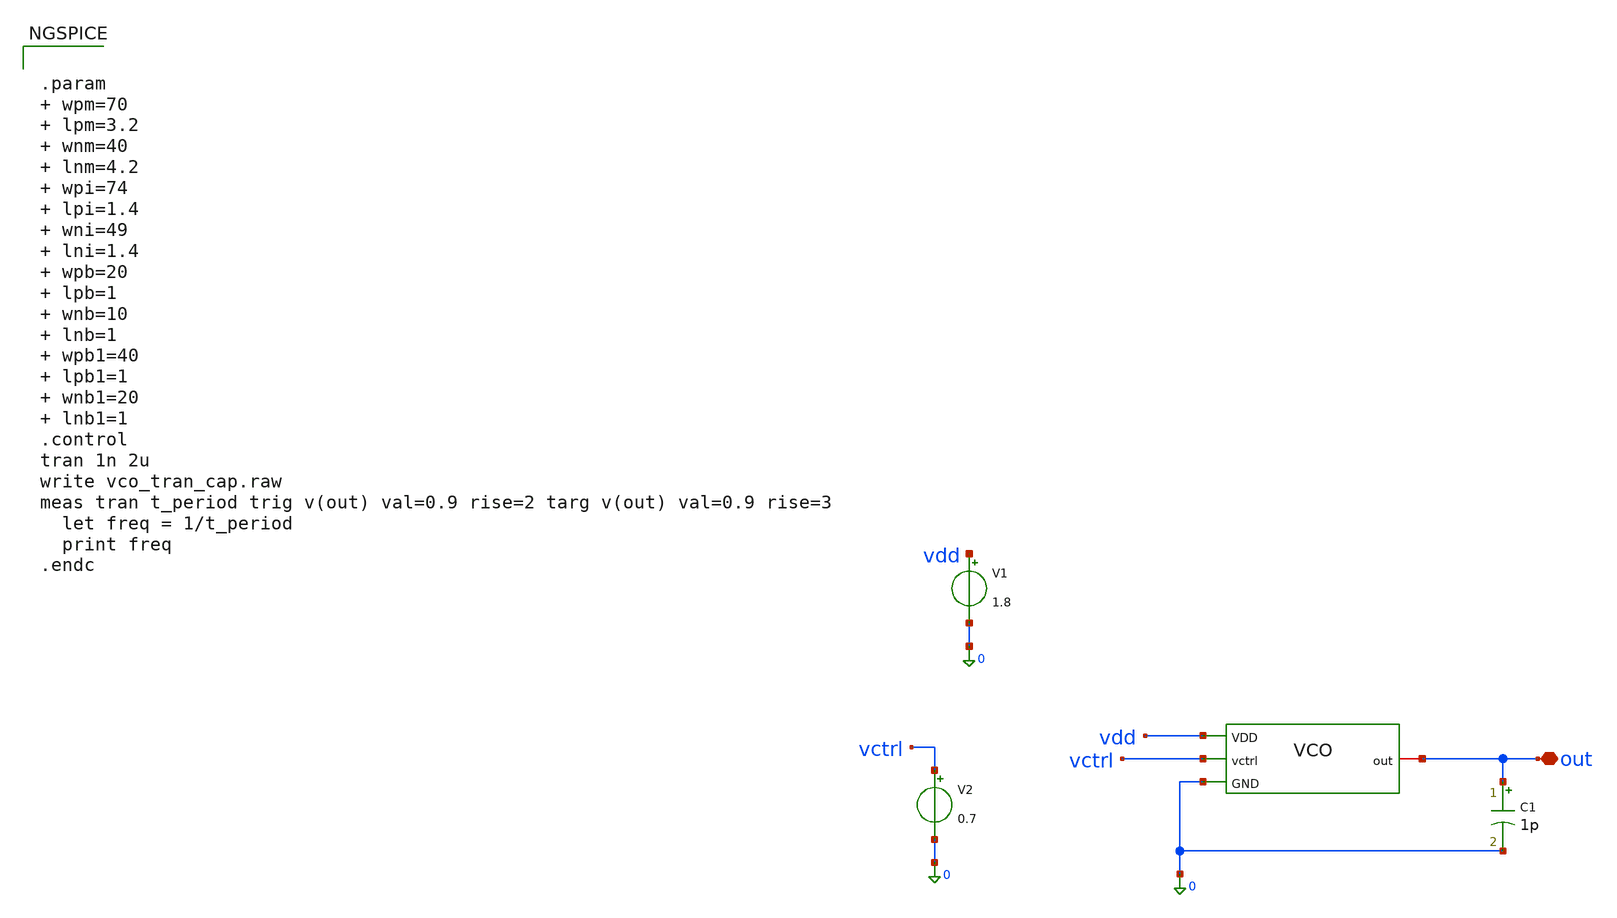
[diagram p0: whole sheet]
** sch_path: design_data/xschem/VCO/vco_tran_cap.sch
**.subckt vco_tran_cap out
*.iopin out
V1 vdd 0 1.8
V2 vctrl 0 0.7
C1 out 0 1p m=1
x1 vdd out vctrl 0 vco
**** begin user architecture code


.param  wpm=70  lpm=3.2  wnm=40  lnm=4.2  wpi=74  lpi=1.4  wni=49  lni=1.4  wpb=20  lpb=1  wnb=10
+  lnb=1  wpb1=40  lpb1=1  wnb1=20  lnb1=1
.control
tran 1n 2u
write vco_tran_cap.raw
meas tran t_period trig v(out) val=0.9 rise=2 targ v(out) val=0.9 rise=3
  let freq = 1/t_period
  print freq
.endc



** opencircuitdesign pdks install
.lib $::SKYWATER_MODELS/sky130.lib.spice ss

**** end user architecture code
**.ends

* expanding   symbol:  xschem/VCO/vco.sym # of pins=4
** sym_path: design_data/xschem/VCO/vco.sym
** sch_path: design_data/xschem/VCO/vco.sch
.subckt vco VDD out vctrl GND
*.ipin vctrl
*.iopin out
*.ipin GND
*.ipin VDD
XM7 net4 net4 VDD VDD sky130_fd_pr__pfet_01v8 L=3.2 W=70 nf=1 ad='int((1 + 1)/2) * 70 / 1 * 0.29' as='int((1 + 2)/2) * 70 / 1 * 0.29'
+ pd='2*int((1 + 1)/2) * (70 / 1 + 0.29)' ps='2*int((1 + 2)/2) * (70 / 1 + 0.29)' nrd='0.29 / 70 ' nrs='0.29 / 70 '
+ sa=0 sb=0 sd=0 mult=1 m=1
XM8 net4 vctrl GND GND sky130_fd_pr__nfet_01v8 L=4.2 W=40 nf=1 ad='int((1 + 1)/2) * 40 / 1 * 0.29' as='int((1 + 2)/2) * 40 / 1 * 0.29'
+ pd='2*int((1 + 1)/2) * (40 / 1 + 0.29)' ps='2*int((1 + 2)/2) * (40 / 1 + 0.29)' nrd='0.29 / 40 ' nrs='0.29 / 40 '
+ sa=0 sb=0 sd=0 mult=1 m=1
XM5 net11 vctrl GND GND sky130_fd_pr__nfet_01v8 L=4.2 W=40 nf=1 ad='int((1 + 1)/2) * 40 / 1 * 0.29' as='int((1 + 2)/2) * 40 / 1 * 0.29'
+ pd='2*int((1 + 1)/2) * (40 / 1 + 0.29)' ps='2*int((1 + 2)/2) * (40 / 1 + 0.29)' nrd='0.29 / 40 ' nrs='0.29 / 40 '
+ sa=0 sb=0 sd=0 mult=1 m=1
XM6 net1 net3 net11 GND sky130_fd_pr__nfet_01v8 L=1.4 W=49 nf=1 ad='int((1 + 1)/2) * 49 / 1 * 0.29' as='int((1 + 2)/2) * 49 / 1 * 0.29'
+ pd='2*int((1 + 1)/2) * (49 / 1 + 0.29)' ps='2*int((1 + 2)/2) * (49 / 1 + 0.29)' nrd='0.29 / 49 ' nrs='0.29 / 49 '
+ sa=0 sb=0 sd=0 mult=1 m=1
XM1 net2 net4 VDD VDD sky130_fd_pr__pfet_01v8 L=3.2 W=70 nf=1 ad='int((1 + 1)/2) * 70 / 1 * 0.29' as='int((1 + 2)/2) * 70 / 1 * 0.29'
+ pd='2*int((1 + 1)/2) * (70 / 1 + 0.29)' ps='2*int((1 + 2)/2) * (70 / 1 + 0.29)' nrd='0.29 / 70 ' nrs='0.29 / 70 '
+ sa=0 sb=0 sd=0 mult=1 m=1
XM2 net1 net3 net2 net2 sky130_fd_pr__pfet_01v8 L=1.4 W=74 nf=1 ad='int((1 + 1)/2) * 74 / 1 * 0.29' as='int((1 + 2)/2) * 74 / 1 * 0.29'
+ pd='2*int((1 + 1)/2) * (74 / 1 + 0.29)' ps='2*int((1 + 2)/2) * (74 / 1 + 0.29)' nrd='0.29 / 74 ' nrs='0.29 / 74 '
+ sa=0 sb=0 sd=0 mult=1 m=1
XM3 net10 vctrl GND GND sky130_fd_pr__nfet_01v8 L=4.2 W=40 nf=1 ad='int((1 + 1)/2) * 40 / 1 * 0.29' as='int((1 + 2)/2) * 40 / 1 * 0.29'
+ pd='2*int((1 + 1)/2) * (40 / 1 + 0.29)' ps='2*int((1 + 2)/2) * (40 / 1 + 0.29)' nrd='0.29 / 40 ' nrs='0.29 / 40 '
+ sa=0 sb=0 sd=0 mult=1 m=1
XM9 net5 net4 VDD VDD sky130_fd_pr__pfet_01v8 L=3.2 W=70 nf=1 ad='int((1 + 1)/2) * 70 / 1 * 0.29' as='int((1 + 2)/2) * 70 / 1 * 0.29'
+ pd='2*int((1 + 1)/2) * (70 / 1 + 0.29)' ps='2*int((1 + 2)/2) * (70 / 1 + 0.29)' nrd='0.29 / 70 ' nrs='0.29 / 70 '
+ sa=0 sb=0 sd=0 mult=1 m=1
XM11 net9 vctrl GND GND sky130_fd_pr__nfet_01v8 L=4.2 W=40 nf=1 ad='int((1 + 1)/2) * 40 / 1 * 0.29' as='int((1 + 2)/2) * 40 / 1 * 0.29'
+ pd='2*int((1 + 1)/2) * (40 / 1 + 0.29)' ps='2*int((1 + 2)/2) * (40 / 1 + 0.29)' nrd='0.29 / 40 ' nrs='0.29 / 40 '
+ sa=0 sb=0 sd=0 mult=1 m=1
XM13 net6 net4 VDD VDD sky130_fd_pr__pfet_01v8 L=3.2 W=70 nf=1 ad='int((1 + 1)/2) * 70 / 1 * 0.29' as='int((1 + 2)/2) * 70 / 1 * 0.29'
+ pd='2*int((1 + 1)/2) * (70 / 1 + 0.29)' ps='2*int((1 + 2)/2) * (70 / 1 + 0.29)' nrd='0.29 / 70 ' nrs='0.29 / 70 '
+ sa=0 sb=0 sd=0 mult=1 m=1
XM4 net7 net1 net10 GND sky130_fd_pr__nfet_01v8 L=1.4 W=49 nf=1 ad='int((1 + 1)/2) * 49 / 1 * 0.29' as='int((1 + 2)/2) * 49 / 1 * 0.29'
+ pd='2*int((1 + 1)/2) * (49 / 1 + 0.29)' ps='2*int((1 + 2)/2) * (49 / 1 + 0.29)' nrd='0.29 / 49 ' nrs='0.29 / 49 '
+ sa=0 sb=0 sd=0 mult=1 m=1
XM10 net7 net1 net5 net5 sky130_fd_pr__pfet_01v8 L=1.4 W=74 nf=1 ad='int((1 + 1)/2) * 74 / 1 * 0.29'
+ as='int((1 + 2)/2) * 74 / 1 * 0.29' pd='2*int((1 + 1)/2) * (74 / 1 + 0.29)' ps='2*int((1 + 2)/2) * (74 / 1 + 0.29)'
+ nrd='0.29 / 74 ' nrs='0.29 / 74 ' sa=0 sb=0 sd=0 mult=1 m=1
XM12 net3 net7 net9 GND sky130_fd_pr__nfet_01v8 L=1.4 W=49 nf=1 ad='int((1 + 1)/2) * 49 / 1 * 0.29' as='int((1 + 2)/2) * 49 / 1 * 0.29'
+ pd='2*int((1 + 1)/2) * (49 / 1 + 0.29)' ps='2*int((1 + 2)/2) * (49 / 1 + 0.29)' nrd='0.29 / 49 ' nrs='0.29 / 49 '
+ sa=0 sb=0 sd=0 mult=1 m=1
XM14 net3 net7 net6 net6 sky130_fd_pr__pfet_01v8 L=1.4 W=74 nf=1 ad='int((1 + 1)/2) * 74 / 1 * 0.29'
+ as='int((1 + 2)/2) * 74 / 1 * 0.29' pd='2*int((1 + 1)/2) * (74 / 1 + 0.29)' ps='2*int((1 + 2)/2) * (74 / 1 + 0.29)'
+ nrd='0.29 / 74 ' nrs='0.29 / 74 ' sa=0 sb=0 sd=0 mult=1 m=1
XM15 net8 net3 GND GND sky130_fd_pr__nfet_01v8 L=1 W=10 nf=1 ad='int((1 + 1)/2) * 10 / 1 * 0.29' as='int((1 + 2)/2) * 10 / 1 * 0.29'
+ pd='2*int((1 + 1)/2) * (10 / 1 + 0.29)' ps='2*int((1 + 2)/2) * (10 / 1 + 0.29)' nrd='0.29 / 10 ' nrs='0.29 / 10 '
+ sa=0 sb=0 sd=0 mult=1 m=1
XM16 net8 net3 VDD VDD sky130_fd_pr__pfet_01v8 L=1 W=20 nf=1 ad='int((1 + 1)/2) * 20 / 1 * 0.29' as='int((1 + 2)/2) * 20 / 1 * 0.29'
+ pd='2*int((1 + 1)/2) * (20 / 1 + 0.29)' ps='2*int((1 + 2)/2) * (20 / 1 + 0.29)' nrd='0.29 / 20 ' nrs='0.29 / 20 '
+ sa=0 sb=0 sd=0 mult=1 m=1
XM17 out net8 GND GND sky130_fd_pr__nfet_01v8 L=1 W=20 nf=1 ad='int((1 + 1)/2) * 20 / 1 * 0.29' as='int((1 + 2)/2) * 20 / 1 * 0.29'
+ pd='2*int((1 + 1)/2) * (20 / 1 + 0.29)' ps='2*int((1 + 2)/2) * (20 / 1 + 0.29)' nrd='0.29 / 20 ' nrs='0.29 / 20 '
+ sa=0 sb=0 sd=0 mult=1 m=1
XM18 out net8 VDD VDD sky130_fd_pr__pfet_01v8 L=1 W=40 nf=1 ad='int((1 + 1)/2) * 40 / 1 * 0.29' as='int((1 + 2)/2) * 40 / 1 * 0.29'
+ pd='2*int((1 + 1)/2) * (40 / 1 + 0.29)' ps='2*int((1 + 2)/2) * (40 / 1 + 0.29)' nrd='0.29 / 40 ' nrs='0.29 / 40 '
+ sa=0 sb=0 sd=0 mult=1 m=1
.ends

.end
